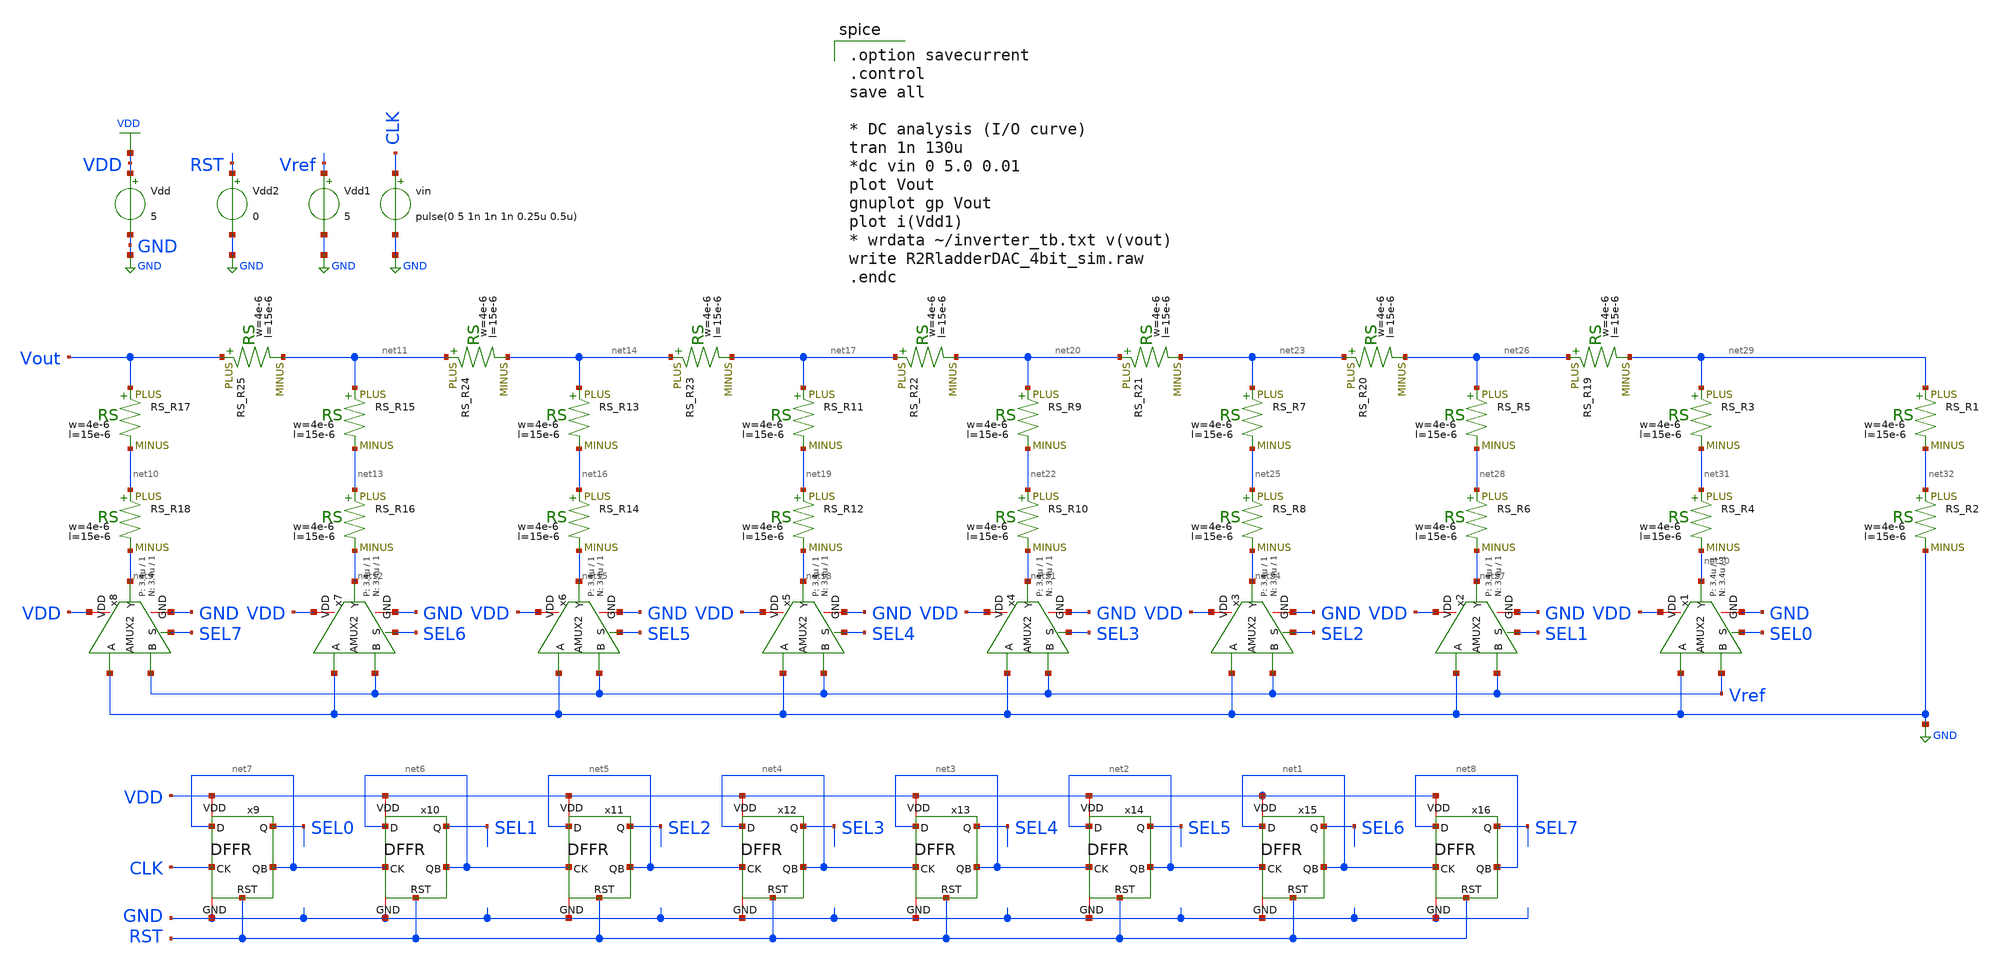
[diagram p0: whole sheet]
** sch_path: IO_202604/09/xschem/R2RladderDAC_8bit_initparam_sim.sch
**.subckt R2RladderDAC_8bit_initparam_sim
Vdd VDD GND 5
Vdd1 Vref GND 5
vin CLK GND pulse(0 5 1n 1n 1n 0.25u 0.5u)
x9 VDD net7 net7 SEL0 RST GND CLK DFFR
x10 VDD net6 net6 SEL1 RST GND net7 DFFR
x11 VDD net5 net5 SEL2 RST GND net6 DFFR
x12 VDD net4 net4 SEL3 RST GND net5 DFFR
x13 VDD net3 net3 SEL4 RST GND net4 DFFR
x14 VDD net2 net2 SEL5 RST GND net3 DFFR
x15 VDD net1 net1 SEL6 RST GND net2 DFFR
x16 VDD net8 net8 SEL7 RST GND net1 DFFR
Vdd2 RST GND 0
x1 VDD Vref net30 SEL0 GND GND AMUX2 WP=3.4u WPM=1 WN=3.4u WNM=1
x2 VDD Vref net27 SEL1 GND GND AMUX2 WP=3.4u WPM=1 WN=3.4u WNM=1
x3 VDD Vref net24 SEL2 GND GND AMUX2 WP=3.4u WPM=1 WN=3.4u WNM=1
x4 VDD Vref net21 SEL3 GND GND AMUX2 WP=3.4u WPM=1 WN=3.4u WNM=1
x5 VDD Vref net18 SEL4 GND GND AMUX2 WP=3.4u WPM=1 WN=3.4u WNM=1
x6 VDD Vref net15 SEL5 GND GND AMUX2 WP=3.4u WPM=1 WN=3.4u WNM=1
x7 VDD Vref net12 SEL6 GND GND AMUX2 WP=3.4u WPM=1 WN=3.4u WNM=1
x8 VDD Vref net9 SEL7 GND GND AMUX2 WP=3.4u WPM=1 WN=3.4u WNM=1
XR1 net29 net32 F_RS w=4e-6 R=1 l=15e-6 tc1=0 tc2=0
XR2 net32 GND F_RS w=4e-6 R=1 l=15e-6 tc1=0 tc2=0
XR3 net29 net31 F_RS w=4e-6 R=1 l=15e-6 tc1=0 tc2=0
XR4 net31 net30 F_RS w=4e-6 R=1 l=15e-6 tc1=0 tc2=0
XR5 net26 net28 F_RS w=4e-6 R=1 l=15e-6 tc1=0 tc2=0
XR6 net28 net27 F_RS w=4e-6 R=1 l=15e-6 tc1=0 tc2=0
XR7 net23 net25 F_RS w=4e-6 R=1 l=15e-6 tc1=0 tc2=0
XR8 net25 net24 F_RS w=4e-6 R=1 l=15e-6 tc1=0 tc2=0
XR9 net20 net22 F_RS w=4e-6 R=1 l=15e-6 tc1=0 tc2=0
XR10 net22 net21 F_RS w=4e-6 R=1 l=15e-6 tc1=0 tc2=0
XR11 net17 net19 F_RS w=4e-6 R=1 l=15e-6 tc1=0 tc2=0
XR12 net19 net18 F_RS w=4e-6 R=1 l=15e-6 tc1=0 tc2=0
XR13 net14 net16 F_RS w=4e-6 R=1 l=15e-6 tc1=0 tc2=0
XR14 net16 net15 F_RS w=4e-6 R=1 l=15e-6 tc1=0 tc2=0
XR15 net11 net13 F_RS w=4e-6 R=1 l=15e-6 tc1=0 tc2=0
XR16 net13 net12 F_RS w=4e-6 R=1 l=15e-6 tc1=0 tc2=0
XR17 Vout net10 F_RS w=4e-6 R=1 l=15e-6 tc1=0 tc2=0
XR18 net10 net9 F_RS w=4e-6 R=1 l=15e-6 tc1=0 tc2=0
XR19 net26 net29 F_RS w=4e-6 R=1 l=15e-6 tc1=0 tc2=0
XR20 net23 net26 F_RS w=4e-6 R=1 l=15e-6 tc1=0 tc2=0
XR21 net20 net23 F_RS w=4e-6 R=1 l=15e-6 tc1=0 tc2=0
XR22 net17 net20 F_RS w=4e-6 R=1 l=15e-6 tc1=0 tc2=0
XR23 net14 net17 F_RS w=4e-6 R=1 l=15e-6 tc1=0 tc2=0
XR24 net11 net14 F_RS w=4e-6 R=1 l=15e-6 tc1=0 tc2=0
XR25 Vout net11 F_RS w=4e-6 R=1 l=15e-6 tc1=0 tc2=0
**** begin user architecture code
 .include $::LIB/../ip62_models

.option savecurrent
.control
save all

* DC analysis (I/O curve)
tran 1n 130u
*dc vin 0 5.0 0.01
plot Vout
gnuplot gp Vout
plot i(Vdd1)
* wrdata ~/inverter_tb.txt v(vout)
write R2RladderDAC_4bit_sim.raw
.endc

**** end user architecture code
**.ends

* expanding   symbol:  IP62_5_stdcell/DFFR.sym # of pins=7
** sym_path: IP62_5_stdcell/DFFR.sym
** sch_path: IP62_5_stdcell/DFFR.sch
.subckt DFFR VDD QB D Q RST GND CK
*.iopin VDD
*.iopin GND
*.ipin CK
*.ipin D
*.opin Q
*.opin QB
*.ipin RST
XM2 net2 D VDD VDD PMOS w=10.2u l=1u as=0 ad=0 ps=0 pd=0 nrd=0 nrs=0 m=1
XM1 net3 CLK net2 VDD PMOS w=10.2u l=1u as=0 ad=0 ps=0 pd=0 nrd=0 nrs=0 m=1
XM11 net5 net8 VDD VDD PMOS w=10.2u l=1u as=0 ad=0 ps=0 pd=0 nrd=0 nrs=0 m=1
XM12 net3 CKB net5 VDD PMOS w=10.2u l=1u as=0 ad=0 ps=0 pd=0 nrd=0 nrs=0 m=1
XM15 net7 net3 VDD VDD PMOS w=10.2u l=1u as=0 ad=0 ps=0 pd=0 nrd=0 nrs=0 m=1
XM16 net8 RST net7 VDD PMOS w=10.2u l=1u as=0 ad=0 ps=0 pd=0 nrd=0 nrs=0 m=1
XM18 net9 net8 VDD VDD PMOS w=10.2u l=1u as=0 ad=0 ps=0 pd=0 nrd=0 nrs=0 m=1
XM19 net10 CKB net9 VDD PMOS w=10.2u l=1u as=0 ad=0 ps=0 pd=0 nrd=0 nrs=0 m=1
XM23 net12 net14 VDD VDD PMOS w=10.2u l=1u as=0 ad=0 ps=0 pd=0 nrd=0 nrs=0 m=1
XM24 net10 CLK net12 VDD PMOS w=10.2u l=1u as=0 ad=0 ps=0 pd=0 nrd=0 nrs=0 m=1
XM27 net15 net10 VDD VDD PMOS w=10.2u l=1u as=0 ad=0 ps=0 pd=0 nrd=0 nrs=0 m=1
XM28 net14 RST net15 VDD PMOS w=10.2u l=1u as=0 ad=0 ps=0 pd=0 nrd=0 nrs=0 m=1
XM31 QB net14 VDD VDD PMOS w=10.2u l=1u as=0 ad=0 ps=0 pd=0 nrd=0 nrs=0 m=1
XM33 Q QB VDD VDD PMOS w=10.2u l=1u as=0 ad=0 ps=0 pd=0 nrd=0 nrs=0 m=1
XM35 QB net14 GND GND NMOS w=3.4u l=1u as=0 ad=0 ps=0 pd=0 nrd=0 nrs=0 m=1
XM32 Q QB GND GND NMOS w=3.4u l=1u as=0 ad=0 ps=0 pd=0 nrd=0 nrs=0 m=1
XM29 net14 RST GND GND NMOS w=3.4u l=1u as=0 ad=0 ps=0 pd=0 nrd=0 nrs=0 m=1
XM30 net14 net10 GND GND NMOS w=3.4u l=1u as=0 ad=0 ps=0 pd=0 nrd=0 nrs=0 m=1
XM25 net10 CKB net13 GND NMOS w=3.4u l=1u as=0 ad=0 ps=0 pd=0 nrd=0 nrs=0 m=1
XM26 net13 net14 GND GND NMOS w=3.4u l=1u as=0 ad=0 ps=0 pd=0 nrd=0 nrs=0 m=1
XM20 net10 CLK net11 GND NMOS w=3.4u l=1u as=0 ad=0 ps=0 pd=0 nrd=0 nrs=0 m=1
XM21 net11 net8 GND GND NMOS w=3.4u l=1u as=0 ad=0 ps=0 pd=0 nrd=0 nrs=0 m=1
XM17 net8 net3 GND GND NMOS w=3.4u l=1u as=0 ad=0 ps=0 pd=0 nrd=0 nrs=0 m=1
XM22 net8 RST GND GND NMOS w=3.4u l=1u as=0 ad=0 ps=0 pd=0 nrd=0 nrs=0 m=1
XM13 net3 CLK net6 GND NMOS w=3.4u l=1u as=0 ad=0 ps=0 pd=0 nrd=0 nrs=0 m=1
XM14 net6 net8 GND GND NMOS w=3.4u l=1u as=0 ad=0 ps=0 pd=0 nrd=0 nrs=0 m=1
XM7 net3 CKB net4 GND NMOS w=3.4u l=1u as=0 ad=0 ps=0 pd=0 nrd=0 nrs=0 m=1
XM8 net4 D GND GND NMOS w=3.4u l=1u as=0 ad=0 ps=0 pd=0 nrd=0 nrs=0 m=1
XM3 net1 CK VDD VDD PMOS w=10.2u l=1u as=0 ad=0 ps=0 pd=0 nrd=0 nrs=0 m=1
XM4 CLK net1 VDD VDD PMOS w=10.2u l=1u as=0 ad=0 ps=0 pd=0 nrd=0 nrs=0 m=1
XM5 CKB CLK VDD VDD PMOS w=10.2u l=1u as=0 ad=0 ps=0 pd=0 nrd=0 nrs=0 m=1
XM34 net1 CK GND GND NMOS w=3.4u l=1u as=0 ad=0 ps=0 pd=0 nrd=0 nrs=0 m=1
XM6 CLK net1 GND GND NMOS w=3.4u l=1u as=0 ad=0 ps=0 pd=0 nrd=0 nrs=0 m=1
XM9 CKB CLK GND GND NMOS w=3.4u l=1u as=0 ad=0 ps=0 pd=0 nrd=0 nrs=0 m=1
.ends


* expanding   symbol:  design/IO_Self-published/AMUX2.sym # of pins=6
** sym_path: Vol.2/files/05/xschem/AMUX2.sym
** sch_path: Vol.2/files/05/xschem/AMUX2.sch
.subckt AMUX2 VDD B Y S A GND  WP=6.8u WPM=1 WN=3.4u WNM=2
*.ipin B
*.ipin S
*.opin Y
*.iopin VDD
*.iopin GND
*.ipin A
XM13 net1 S VDD VDD PMOS w=6.8u l=1u as=0 ad=0 ps=0 pd=0 nrd=0 nrs=0 m=1
XM8 Y net1 B VDD PMOS w=WP l=1u as=0 ad=0 ps=0 pd=0 nrd=0 nrs=0 m=WPM
XM2 Y net2 A VDD PMOS w=WP l=1u as=0 ad=0 ps=0 pd=0 nrd=0 nrs=0 m=WPM
XM12 net1 S GND GND NMOS w=3.4u l=1u as=0 ad=0 ps=0 pd=0 nrd=0 nrs=0 m=1
XM6 Y net2 B GND NMOS w=WN l=1u as=0 ad=0 ps=0 pd=0 nrd=0 nrs=0 m=WNM
XM4 Y net1 A GND NMOS w=WN l=1u as=0 ad=0 ps=0 pd=0 nrd=0 nrs=0 m=WNM
XM1 net2 GND S VDD PMOS w=6.8u l=1u as=0 ad=0 ps=0 pd=0 nrd=0 nrs=0 m=1
XM3 net2 VDD S GND NMOS w=3.4u l=1u as=0 ad=0 ps=0 pd=0 nrd=0 nrs=0 m=1
.ends

.GLOBAL GND
.GLOBAL VDD
.end
